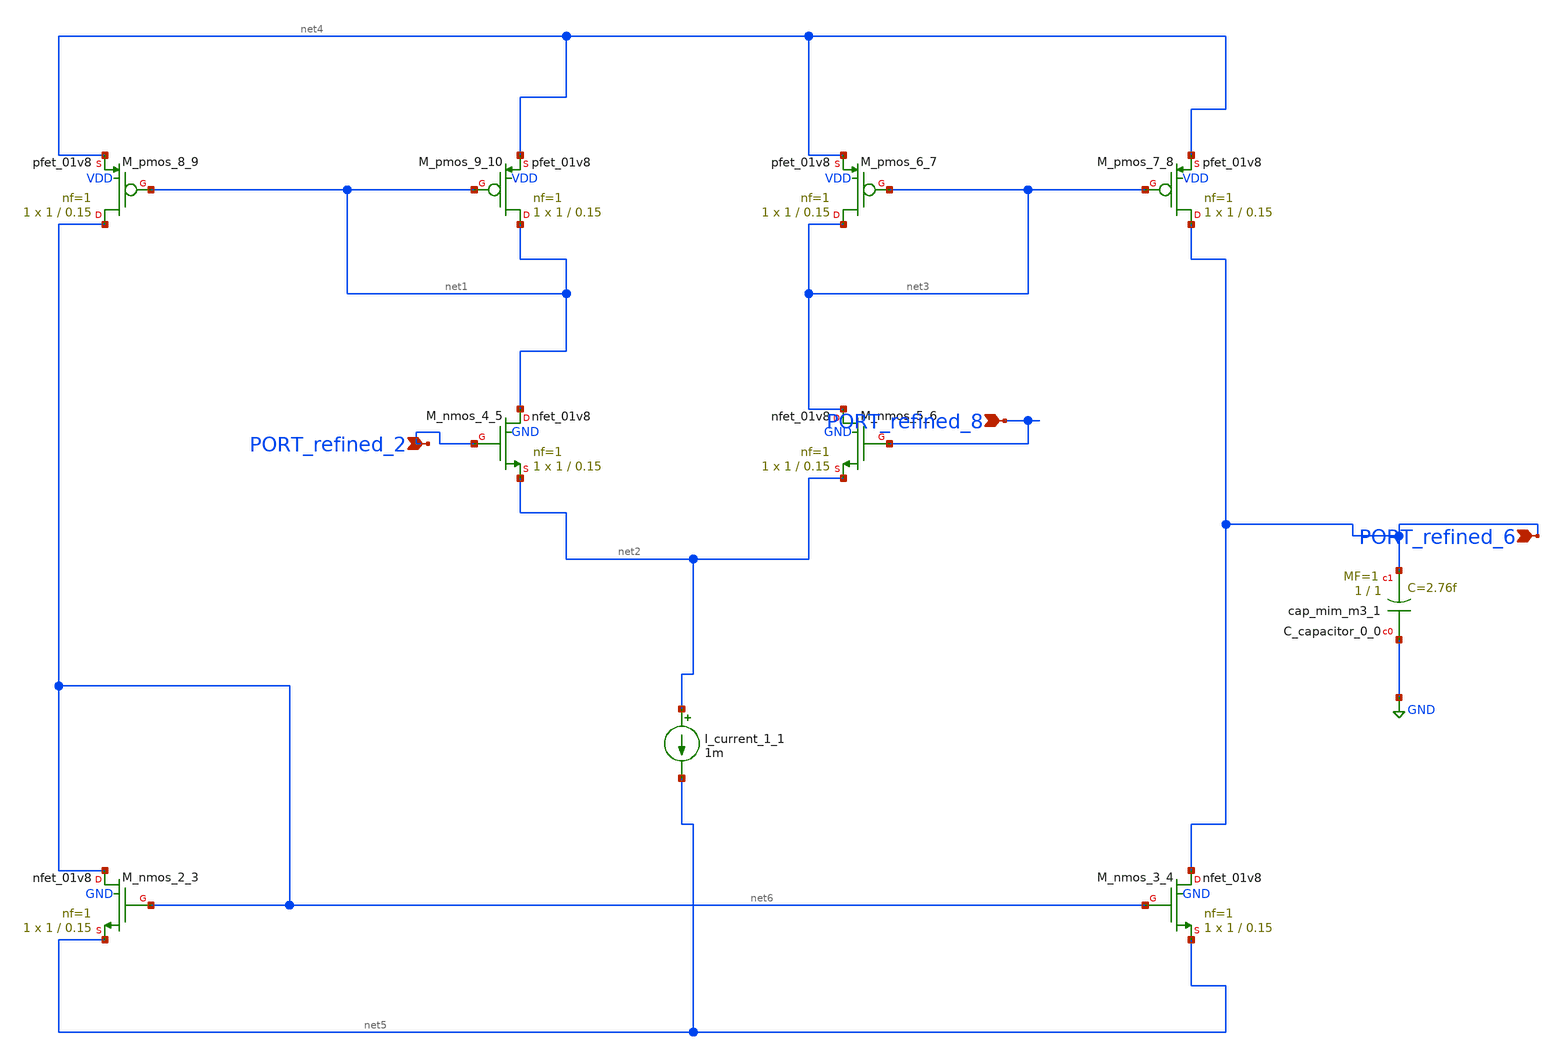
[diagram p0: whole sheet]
** sch_path: schematics/SchemGen/10_11591_ijeecs_v14_i1_pp230-240_03_001.sch
**.subckt 10_11591_ijeecs_v14_i1_pp230-240_03_001 PORT_refined_6 PORT_refined_2 PORT_refined_8
*.ipin PORT_refined_6
*.ipin PORT_refined_2
*.ipin PORT_refined_8
XC_capacitor_0_0 GND PORT_refined_6 sky130_fd_pr__cap_mim_m3_1 W=1 L=1 MF=1 m=1
I_current_1_1 net2 net5 1m
XM_nmos_2_3 net6 net6 net5 GND sky130_fd_pr__nfet_01v8 L=0.15 W=1 nf=1 ad='int((1 + 1)/2) * 1 / 1 * 0.29'
+ as='int((1 + 2)/2) * 1 / 1 * 0.29' pd='2*int((1 + 1)/2) * (1 / 1 + 0.29)' ps='2*int((1 + 2)/2) * (1 / 1 + 0.29)'
+ nrd='0.29 / 1 ' nrs='0.29 / 1 ' sa=0 sb=0 sd=0 mult=1 m=1
XM_nmos_3_4 PORT_refined_6 net6 net5 GND sky130_fd_pr__nfet_01v8 L=0.15 W=1 nf=1 ad='int((1 + 1)/2) * 1 / 1 * 0.29'
+ as='int((1 + 2)/2) * 1 / 1 * 0.29' pd='2*int((1 + 1)/2) * (1 / 1 + 0.29)' ps='2*int((1 + 2)/2) * (1 / 1 + 0.29)'
+ nrd='0.29 / 1 ' nrs='0.29 / 1 ' sa=0 sb=0 sd=0 mult=1 m=1
XM_nmos_4_5 net1 PORT_refined_2 net2 GND sky130_fd_pr__nfet_01v8 L=0.15 W=1 nf=1 ad='int((1 + 1)/2) * 1 / 1 * 0.29'
+ as='int((1 + 2)/2) * 1 / 1 * 0.29' pd='2*int((1 + 1)/2) * (1 / 1 + 0.29)' ps='2*int((1 + 2)/2) * (1 / 1 + 0.29)'
+ nrd='0.29 / 1 ' nrs='0.29 / 1 ' sa=0 sb=0 sd=0 mult=1 m=1
XM_nmos_5_6 net3 PORT_refined_8 net2 GND sky130_fd_pr__nfet_01v8 L=0.15 W=1 nf=1 ad='int((1 + 1)/2) * 1 / 1 * 0.29'
+ as='int((1 + 2)/2) * 1 / 1 * 0.29' pd='2*int((1 + 1)/2) * (1 / 1 + 0.29)' ps='2*int((1 + 2)/2) * (1 / 1 + 0.29)'
+ nrd='0.29 / 1 ' nrs='0.29 / 1 ' sa=0 sb=0 sd=0 mult=1 m=1
XM_pmos_6_7 net3 net3 net4 VDD sky130_fd_pr__pfet_01v8 L=0.15 W=1 nf=1 ad='int((1 + 1)/2) * 1 / 1 * 0.29'
+ as='int((1 + 2)/2) * 1 / 1 * 0.29' pd='2*int((1 + 1)/2) * (1 / 1 + 0.29)' ps='2*int((1 + 2)/2) * (1 / 1 + 0.29)'
+ nrd='0.29 / 1 ' nrs='0.29 / 1 ' sa=0 sb=0 sd=0 mult=1 m=1
XM_pmos_7_8 PORT_refined_6 net3 net4 VDD sky130_fd_pr__pfet_01v8 L=0.15 W=1 nf=1 ad='int((1 + 1)/2) * 1 / 1 * 0.29'
+ as='int((1 + 2)/2) * 1 / 1 * 0.29' pd='2*int((1 + 1)/2) * (1 / 1 + 0.29)' ps='2*int((1 + 2)/2) * (1 / 1 + 0.29)'
+ nrd='0.29 / 1 ' nrs='0.29 / 1 ' sa=0 sb=0 sd=0 mult=1 m=1
XM_pmos_8_9 net6 net1 net4 VDD sky130_fd_pr__pfet_01v8 L=0.15 W=1 nf=1 ad='int((1 + 1)/2) * 1 / 1 * 0.29'
+ as='int((1 + 2)/2) * 1 / 1 * 0.29' pd='2*int((1 + 1)/2) * (1 / 1 + 0.29)' ps='2*int((1 + 2)/2) * (1 / 1 + 0.29)'
+ nrd='0.29 / 1 ' nrs='0.29 / 1 ' sa=0 sb=0 sd=0 mult=1 m=1
XM_pmos_9_10 net1 net1 net4 VDD sky130_fd_pr__pfet_01v8 L=0.15 W=1 nf=1 ad='int((1 + 1)/2) * 1 / 1 * 0.29'
+ as='int((1 + 2)/2) * 1 / 1 * 0.29' pd='2*int((1 + 1)/2) * (1 / 1 + 0.29)' ps='2*int((1 + 2)/2) * (1 / 1 + 0.29)'
+ nrd='0.29 / 1 ' nrs='0.29 / 1 ' sa=0 sb=0 sd=0 mult=1 m=1
**.ends
.GLOBAL GND
.end
